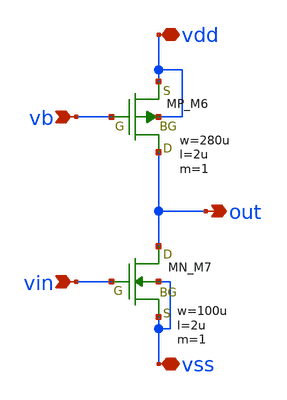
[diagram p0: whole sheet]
** sch_path: member_project/opamp/houta/cs.sch
**.subckt cs vb vin out vss vdd
*.ipin vb
*.ipin vin
*.opin out
*.iopin vss
*.iopin vdd
XM6 out vb vdd vdd PMOS w=280u l=2u as=0 ad=0 ps=0 pd=0 nrd=0 nrs=0 m=1
XM7 out vin vss vss NMOS w=100u l=2u as=0 ad=0 ps=0 pd=0 nrd=0 nrs=0 m=1
**.ends
.end
